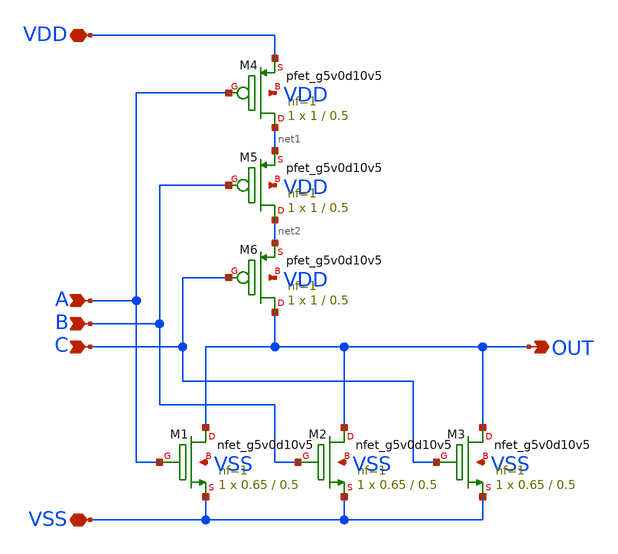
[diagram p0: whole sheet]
** sch_path: xschem/nor3.sch
**.subckt nor3 VSS VDD B A C OUT
*.iopin VSS
*.iopin VDD
*.ipin B
*.ipin A
*.ipin C
*.opin OUT
XM2 OUT B VSS VSS sky130_fd_pr__nfet_g5v0d10v5 L=0.5 W=0.65 nf=1 ad='int((1 + 1)/2) * 0.65 / 1 * 0.29'
+ as='int((1 + 2)/2) * 0.65 / 1 * 0.29' pd='2*int((1 + 1)/2) * (0.65 / 1 + 0.29)' ps='2*int((1 + 2)/2) * (0.65 / 1 + 0.29)'
+ nrd='0.29 / 0.65 ' nrs='0.29 / 0.65 ' sa=0 sb=0 sd=0 mult=1 m=1
XM1 OUT A VSS VSS sky130_fd_pr__nfet_g5v0d10v5 L=0.5 W=0.65 nf=1 ad='int((1 + 1)/2) * 0.65 / 1 * 0.29'
+ as='int((1 + 2)/2) * 0.65 / 1 * 0.29' pd='2*int((1 + 1)/2) * (0.65 / 1 + 0.29)' ps='2*int((1 + 2)/2) * (0.65 / 1 + 0.29)'
+ nrd='0.29 / 0.65 ' nrs='0.29 / 0.65 ' sa=0 sb=0 sd=0 mult=1 m=1
XM4 net1 A VDD VDD sky130_fd_pr__pfet_g5v0d10v5 L=0.5 W=1 nf=1 ad='int((1 + 1)/2) * 1 / 1 * 0.29' as='int((1 + 2)/2) * 1 / 1 * 0.29'
+ pd='2*int((1 + 1)/2) * (1 / 1 + 0.29)' ps='2*int((1 + 2)/2) * (1 / 1 + 0.29)' nrd='0.29 / 1 ' nrs='0.29 / 1 '
+ sa=0 sb=0 sd=0 mult=1 m=1
XM3 OUT C VSS VSS sky130_fd_pr__nfet_g5v0d10v5 L=0.5 W=0.65 nf=1 ad='int((1 + 1)/2) * 0.65 / 1 * 0.29'
+ as='int((1 + 2)/2) * 0.65 / 1 * 0.29' pd='2*int((1 + 1)/2) * (0.65 / 1 + 0.29)' ps='2*int((1 + 2)/2) * (0.65 / 1 + 0.29)'
+ nrd='0.29 / 0.65 ' nrs='0.29 / 0.65 ' sa=0 sb=0 sd=0 mult=1 m=1
XM5 net2 B net1 VDD sky130_fd_pr__pfet_g5v0d10v5 L=0.5 W=1 nf=1 ad='int((1 + 1)/2) * 1 / 1 * 0.29' as='int((1 + 2)/2) * 1 / 1 * 0.29'
+ pd='2*int((1 + 1)/2) * (1 / 1 + 0.29)' ps='2*int((1 + 2)/2) * (1 / 1 + 0.29)' nrd='0.29 / 1 ' nrs='0.29 / 1 '
+ sa=0 sb=0 sd=0 mult=1 m=1
XM6 OUT C net2 VDD sky130_fd_pr__pfet_g5v0d10v5 L=0.5 W=1 nf=1 ad='int((1 + 1)/2) * 1 / 1 * 0.29' as='int((1 + 2)/2) * 1 / 1 * 0.29'
+ pd='2*int((1 + 1)/2) * (1 / 1 + 0.29)' ps='2*int((1 + 2)/2) * (1 / 1 + 0.29)' nrd='0.29 / 1 ' nrs='0.29 / 1 '
+ sa=0 sb=0 sd=0 mult=1 m=1
**.ends
.end
